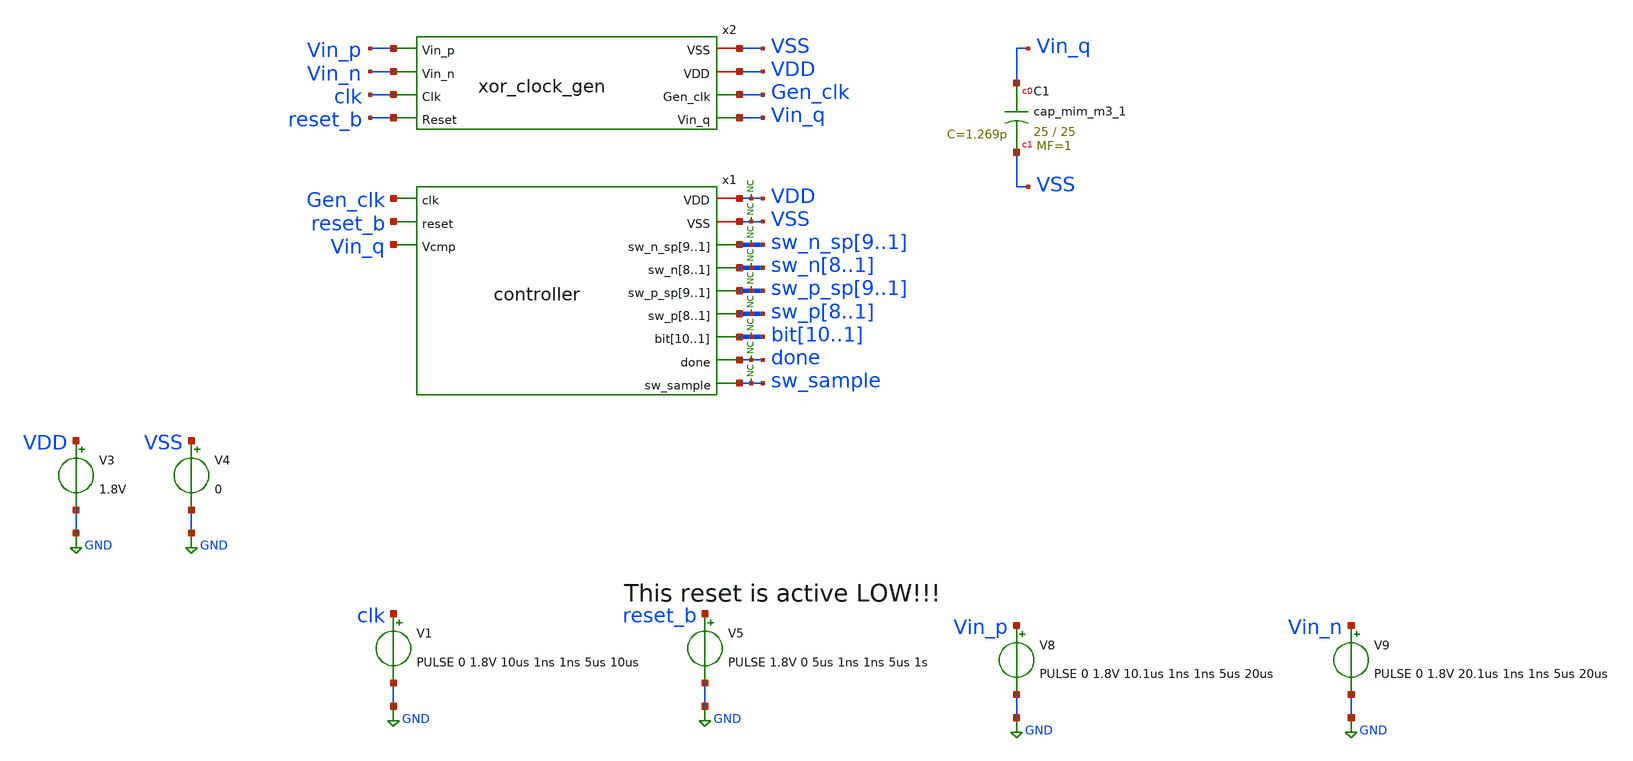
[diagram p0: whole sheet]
** sch_path: xschem/tests/controller/controller_test2.sch
**.subckt controller_test2
V3 VDD GND 1.8V
V4 VSS GND 0
x1 VDD VSS sw_n_sp9 sw_n_sp8 sw_n_sp7 sw_n_sp6 sw_n_sp5 sw_n_sp4 sw_n_sp3 sw_n_sp2 sw_n_sp1 Gen_clk
+ reset_b sw_n8 sw_n7 sw_n6 sw_n5 sw_n4 sw_n3 sw_n2 sw_n1 Vin_q sw_p_sp9 sw_p_sp8 sw_p_sp7 sw_p_sp6 sw_p_sp5
+ sw_p_sp4 sw_p_sp3 sw_p_sp2 sw_p_sp1 sw_p8 sw_p7 sw_p6 sw_p5 sw_p4 sw_p3 sw_p2 sw_p1 bit10 bit9 bit8 bit7
+ bit6 bit5 bit4 bit3 bit2 bit1 done sw_sample controller
V1 clk GND PULSE 0 1.8V 10us 1ns 1ns 5us 10us
V5 reset_b GND PULSE 1.8V 0 5us 1ns 1ns 5us 1s
x2 VSS Vin_p VDD Vin_n Gen_clk clk Vin_q reset_b xor_clock_gen
V8 Vin_p GND PULSE 0 1.8V 10.1us 1ns 1ns 5us 20us
V9 Vin_n GND PULSE 0 1.8V 20.1us 1ns 1ns 5us 20us
* noconn VDD
* noconn VSS
* noconn sw_n_sp[9..1]
* noconn sw_n[8..1]
* noconn sw_p_sp[9..1]
* noconn sw_p[8..1]
* noconn bit[10..1]
* noconn done
* noconn sw_sample
XC1 Vin_q VSS sky130_fd_pr__cap_mim_m3_1 W=25 L=25 MF=1 m=1
**** begin user architecture code
 .lib $::SKYWATER_MODELS/sky130.lib.spice tt
.include $::SKYWATER_STDCELLS/sky130_fd_sc_hd.spice


.options acct list
.temp 25
*vvcc VDD 0 dc 1.8
*vvss VSS 0 0
.control
tran 0.8u 400u
*plot RST_PLS clk+2 Pulse+4
plot done-4  sw_n_sp1 sw_n_sp2+2 sw_n_sp3+4 sw_n_sp4+6 sw_n_sp5+8 sw_n_sp6+10 sw_n_sp7+12
+ sw_n_sp8+14 sw_n_sp9+16 Vin_p+18 clk+20
plot done-4  sw_p_sp1 sw_p_sp2+2 sw_p_sp3+4 sw_p_sp4+6 sw_p_sp5+8 sw_p_sp6+10 sw_p_sp7+12
+ sw_p_sp8+14 sw_p_sp9+16 Vin_p+18 clk+20
plot done-4  sw_n1 sw_n2+2 sw_n3+4 sw_n4+6 sw_n5+8 sw_n6+10 sw_n7+12 sw_n8+14 Vin_p+16 clk+18
plot done-4  sw_p1 sw_p2+2 sw_p3+4 sw_p4+6 sw_p5+8 sw_p6+10 sw_p7+12 sw_p8+14 Vin_p+16 clk+18
plot done-4 bit1 bit2+2 bit3+4 bit4+6 bit5+8 bit6+10 bit7+12 bit8+14 bit9+16 bit10+18

plot done-4  sw_n_sp1 sw_n_sp2+2 sw_n_sp3+4 sw_n_sp4+6 sw_n_sp5+8 sw_n_sp6+10 sw_n_sp7+12
+ sw_n_sp8+14 sw_n_sp9+16 Vin_q+18 clk+20 sw_n1 sw_n2+2 sw_n3+4 sw_n4+6 sw_n5+8 sw_n6+10 sw_n7+12 sw_n8+14

plot done-4  sw_p_sp1 sw_p_sp2+2 sw_p_sp3+4 sw_p_sp4+6 sw_p_sp5+8 sw_p_sp6+10 sw_p_sp7+12
+ sw_p_sp8+14 sw_p_sp9+16 Vin_q+18 clk+20 sw_p1 sw_p2+2 sw_p3+4 sw_p4+6 sw_p5+8 sw_p6+10 sw_p7+12 sw_p8+14

plot clk reset_b+2 x1.cycle0+4 x1.cycle1+6 x1.cycle2+8 x1.cycle16+10 x1.cycle17+12 x1.cycle18+14
+ sw_sample+16 vin_p+18

plot reset_b-2 clk vin_p vin_n gen_clk

plot x1.q_test1 x1.q_test2 x1.cycle3+2 x1.cycle2+4
write controller_test.raw
.endc


**** end user architecture code
**.ends
.GLOBAL GND
.end
